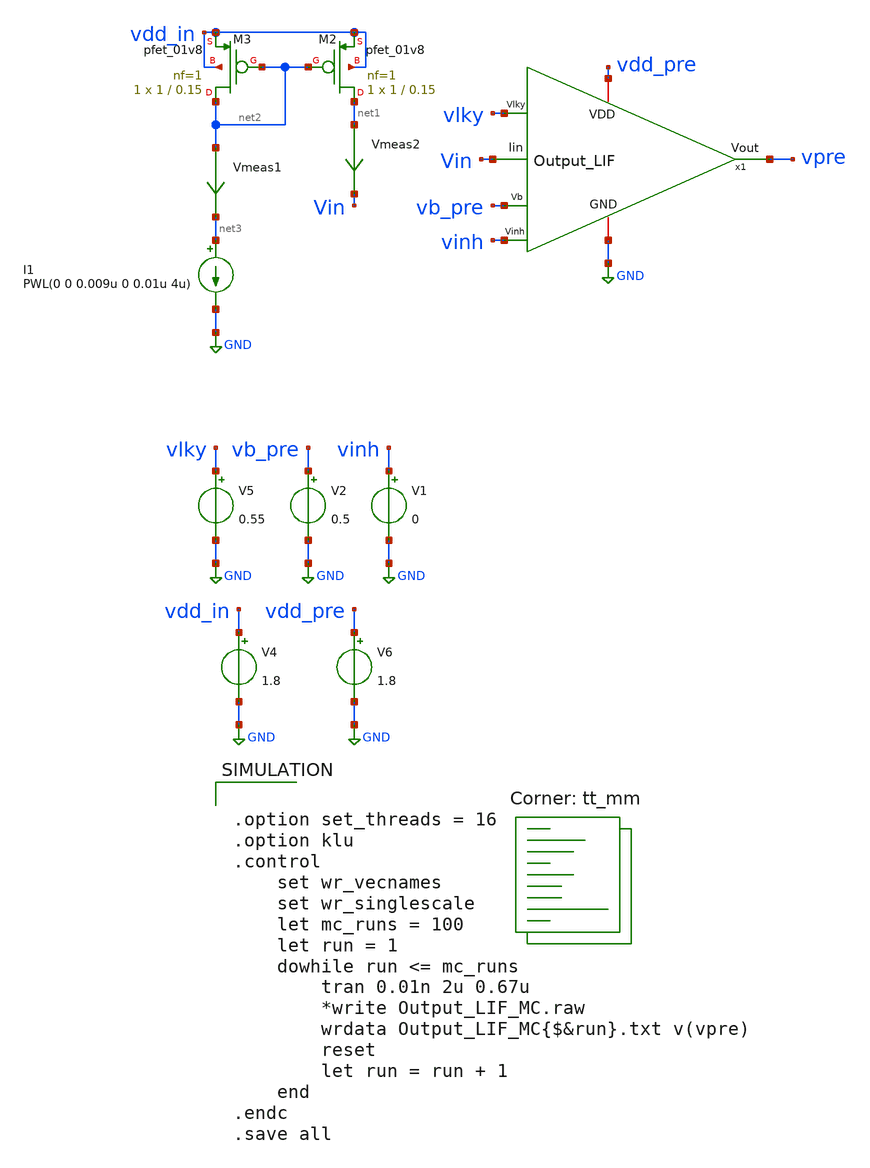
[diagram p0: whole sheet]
** sch_path: SNN/Output_LIF_MC_tb.sch
**.subckt Output_LIF_MC_tb
V2 vb_pre GND 0.5
I1 net3 GND PWL(0 0 0.009u 0 0.01u 4u)
XM2 net1 net2 vdd_in vdd_in sky130_fd_pr__pfet_01v8 L=0.15 W=1 nf=1 ad='int((nf+1)/2) * W/nf * 0.29'
+ as='int((nf+2)/2) * W/nf * 0.29' pd='2*int((nf+1)/2) * (W/nf + 0.29)' ps='2*int((nf+2)/2) * (W/nf + 0.29)'
+ nrd='0.29 / W' nrs='0.29 / W' sa=0 sb=0 sd=0 mult=1 m=1
XM3 net2 net2 vdd_in vdd_in sky130_fd_pr__pfet_01v8 L=0.15 W=1 nf=1 ad='int((nf+1)/2) * W/nf * 0.29'
+ as='int((nf+2)/2) * W/nf * 0.29' pd='2*int((nf+1)/2) * (W/nf + 0.29)' ps='2*int((nf+2)/2) * (W/nf + 0.29)'
+ nrd='0.29 / W' nrs='0.29 / W' sa=0 sb=0 sd=0 mult=1 m=1
Vmeas1 net2 net3 0
.save i(vmeas1)
Vmeas2 net1 Vin 0
.save i(vmeas2)
V4 vdd_in GND 1.8
V5 vlky GND 0.55
V6 vdd_pre GND 1.8
x1 vinh vlky vb_pre vdd_pre vpre GND Vin Output_LIF
V1 vinh GND 0
**** begin user architecture code


.option set_threads = 16
.option klu
.control
	set wr_vecnames
	set wr_singlescale
	let mc_runs = 100
	let run = 1
	dowhile run <= mc_runs
		tran 0.01n 2u 0.67u
		*write Output_LIF_MC.raw
		wrdata Output_LIF_MC{$&run}.txt v(vpre)
		reset
		let run = run + 1
	end
.endc
.save all


.lib $::SKYWATER_MODELS/sky130.lib.spice tt_mm
**** end user architecture code
**.ends

* expanding   symbol:  /home/ricardo/RATT_repos/Proyectos_xschem/SNN/Output_LIF.sym # of pins=7
** sym_path: Final_Design/Output_LIF.sym
** sch_path: Final_Design/Output_LIF.sch
.subckt Output_LIF Vinh Vlky Vb VDD Vout GND Iin
*.iopin GND
*.ipin Vb
*.iopin VDD
*.opin Vout
*.ipin Iin
*.ipin Vlky
*.ipin Vinh
XM5 net3 Vb GND GND sky130_fd_pr__nfet_01v8 L=0.5 W=5 nf=1 ad='int((nf+1)/2) * W/nf * 0.29' as='int((nf+2)/2) * W/nf * 0.29'
+ pd='2*int((nf+1)/2) * (W/nf + 0.29)' ps='2*int((nf+2)/2) * (W/nf + 0.29)' nrd='0.29 / W' nrs='0.29 / W'
+ sa=0 sb=0 sd=0 mult=1 m=1
XM4 net1 net2 net3 GND sky130_fd_pr__nfet_01v8 L=0.15 W=1.5 nf=1 ad='int((nf+1)/2) * W/nf * 0.29' as='int((nf+2)/2) * W/nf * 0.29'
+ pd='2*int((nf+1)/2) * (W/nf + 0.29)' ps='2*int((nf+2)/2) * (W/nf + 0.29)' nrd='0.29 / W' nrs='0.29 / W'
+ sa=0 sb=0 sd=0 mult=1 m=1
XM3 net1 net2 VDD VDD sky130_fd_pr__pfet_01v8 L=5 W=0.5 nf=1 ad='int((nf+1)/2) * W/nf * 0.29' as='int((nf+2)/2) * W/nf * 0.29'
+ pd='2*int((nf+1)/2) * (W/nf + 0.29)' ps='2*int((nf+2)/2) * (W/nf + 0.29)' nrd='0.29 / W' nrs='0.29 / W'
+ sa=0 sb=0 sd=0 mult=1 m=1
XC2 net1 GND sky130_fd_pr__cap_mim_m3_1 W=20 L=20 MF=1 m=1
XM2 Iin net1 GND GND sky130_fd_pr__nfet_01v8 L=0.5 W=5 nf=1 ad='int((nf+1)/2) * W/nf * 0.29' as='int((nf+2)/2) * W/nf * 0.29'
+ pd='2*int((nf+1)/2) * (W/nf + 0.29)' ps='2*int((nf+2)/2) * (W/nf + 0.29)' nrd='0.29 / W' nrs='0.29 / W'
+ sa=0 sb=0 sd=0 mult=1 m=1
XC1 Iin GND sky130_fd_pr__cap_mim_m3_1 W=20 L=10 MF=1 m=1
XM10 net4 Vout GND GND sky130_fd_pr__nfet_01v8 L=0.15 W=1.5 nf=1 ad='int((nf+1)/2) * W/nf * 0.29' as='int((nf+2)/2) * W/nf * 0.29'
+ pd='2*int((nf+1)/2) * (W/nf + 0.29)' ps='2*int((nf+2)/2) * (W/nf + 0.29)' nrd='0.29 / W' nrs='0.29 / W'
+ sa=0 sb=0 sd=0 mult=1 m=1
XM7 net2 Iin net4 GND sky130_fd_pr__nfet_01v8 L=0.15 W=1.5 nf=1 ad='int((nf+1)/2) * W/nf * 0.29' as='int((nf+2)/2) * W/nf * 0.29'
+ pd='2*int((nf+1)/2) * (W/nf + 0.29)' ps='2*int((nf+2)/2) * (W/nf + 0.29)' nrd='0.29 / W' nrs='0.29 / W'
+ sa=0 sb=0 sd=0 mult=1 m=1
XM6 net2 Iin VDD VDD sky130_fd_pr__pfet_01v8 L=0.15 W=1.5 nf=1 ad='int((nf+1)/2) * W/nf * 0.29' as='int((nf+2)/2) * W/nf * 0.29'
+ pd='2*int((nf+1)/2) * (W/nf + 0.29)' ps='2*int((nf+2)/2) * (W/nf + 0.29)' nrd='0.29 / W' nrs='0.29 / W'
+ sa=0 sb=0 sd=0 mult=1 m=1
XM9 Vout net2 net4 GND sky130_fd_pr__nfet_01v8 L=0.15 W=1.5 nf=1 ad='int((nf+1)/2) * W/nf * 0.29' as='int((nf+2)/2) * W/nf * 0.29'
+ pd='2*int((nf+1)/2) * (W/nf + 0.29)' ps='2*int((nf+2)/2) * (W/nf + 0.29)' nrd='0.29 / W' nrs='0.29 / W'
+ sa=0 sb=0 sd=0 mult=1 m=1
XM8 Vout net2 VDD VDD sky130_fd_pr__pfet_01v8 L=0.15 W=5 nf=1 ad='int((nf+1)/2) * W/nf * 0.29' as='int((nf+2)/2) * W/nf * 0.29'
+ pd='2*int((nf+1)/2) * (W/nf + 0.29)' ps='2*int((nf+2)/2) * (W/nf + 0.29)' nrd='0.29 / W' nrs='0.29 / W'
+ sa=0 sb=0 sd=0 mult=1 m=1
XM1 Iin Vlky GND GND sky130_fd_pr__nfet_01v8 L=0.15 W=1.5 nf=1 ad='int((nf+1)/2) * W/nf * 0.29' as='int((nf+2)/2) * W/nf * 0.29'
+ pd='2*int((nf+1)/2) * (W/nf + 0.29)' ps='2*int((nf+2)/2) * (W/nf + 0.29)' nrd='0.29 / W' nrs='0.29 / W'
+ sa=0 sb=0 sd=0 mult=1 m=1
XM11 VDD Vinh net1 GND sky130_fd_pr__nfet_01v8 L=0.15 W=1 nf=1 ad='int((nf+1)/2) * W/nf * 0.29' as='int((nf+2)/2) * W/nf * 0.29'
+ pd='2*int((nf+1)/2) * (W/nf + 0.29)' ps='2*int((nf+2)/2) * (W/nf + 0.29)' nrd='0.29 / W' nrs='0.29 / W'
+ sa=0 sb=0 sd=0 mult=1 m=1
.ends

.GLOBAL GND
.end
